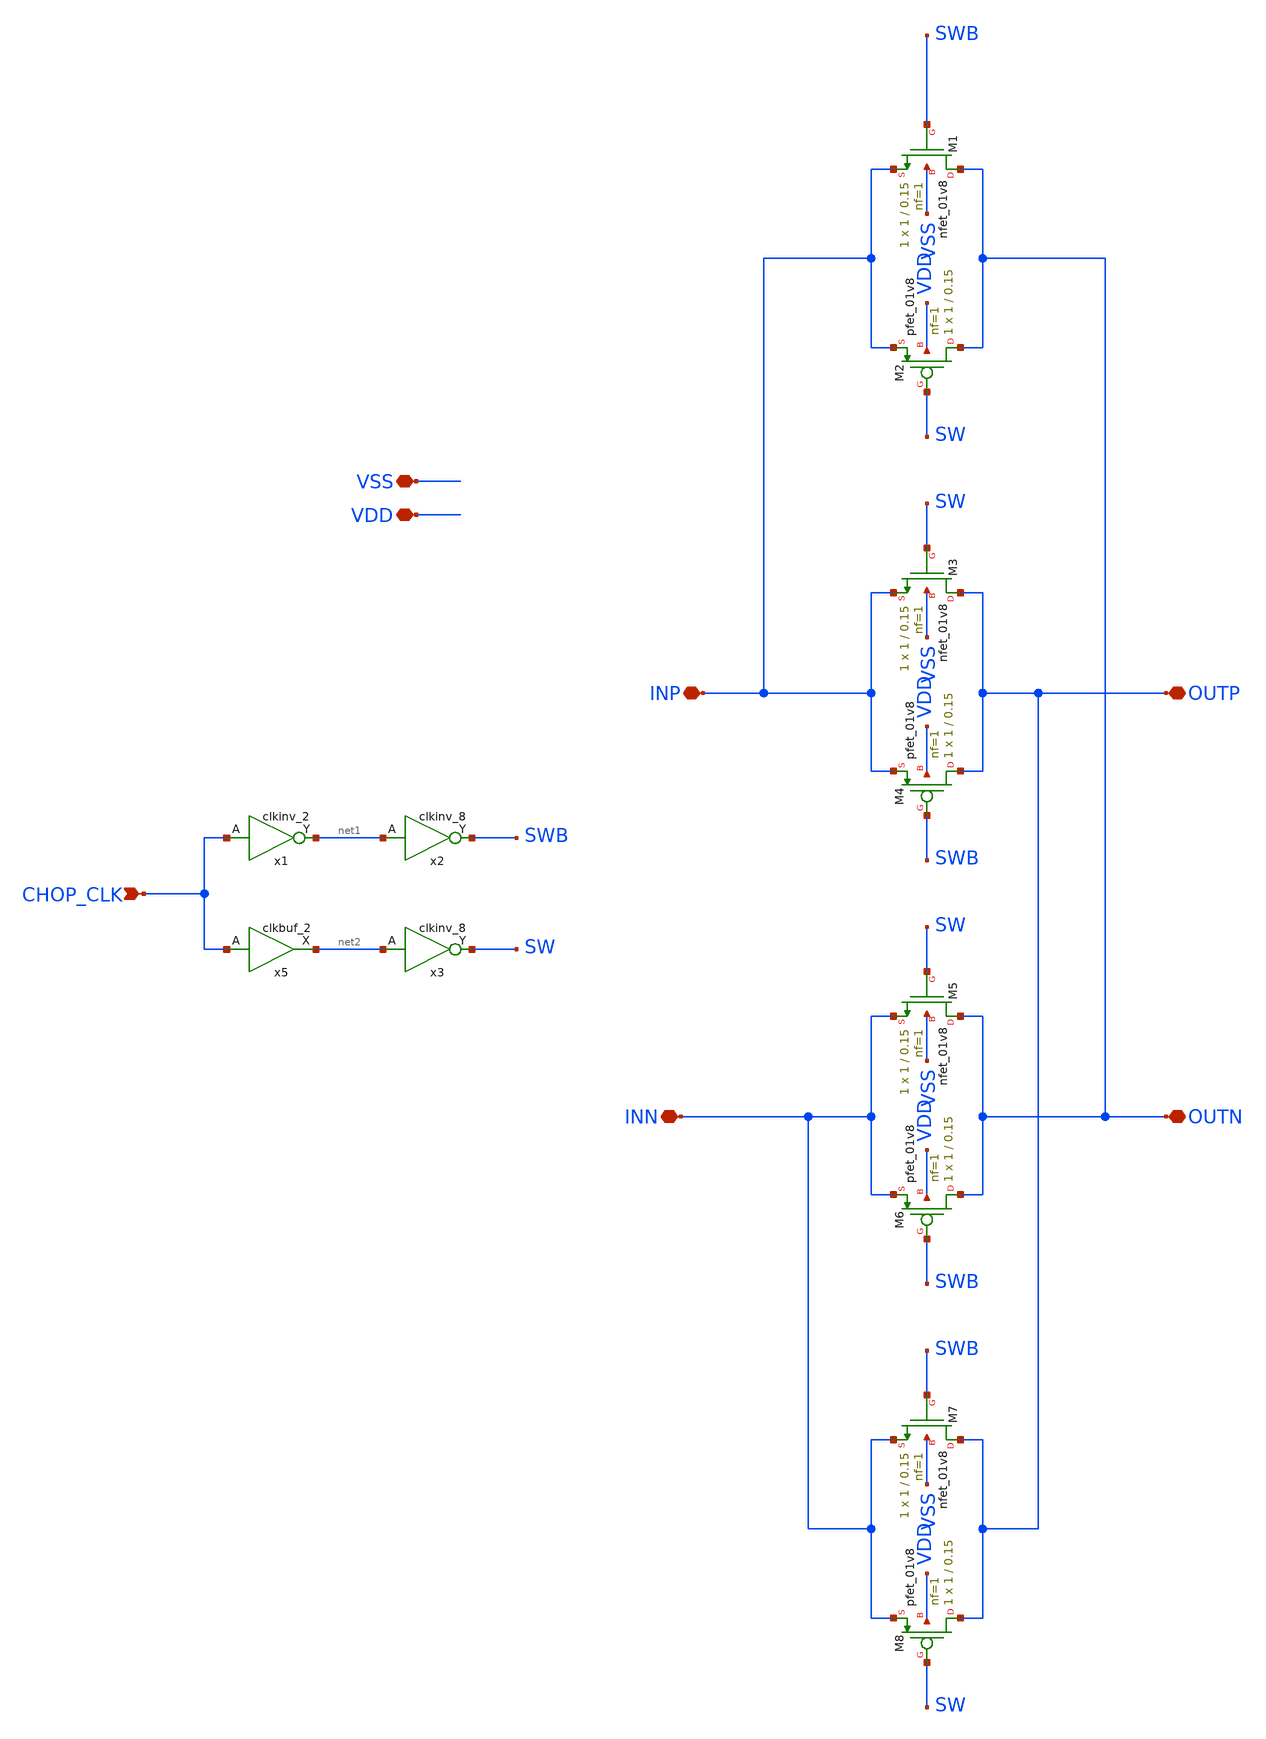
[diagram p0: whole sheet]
** sch_path: opamp_lna/chopper.sch
**.subckt chopper CHOP_CLK INP INN OUTP OUTN VSS VDD
*.ipin CHOP_CLK
*.iopin INP
*.iopin INN
*.iopin OUTP
*.iopin OUTN
*.iopin VSS
*.iopin VDD
XM1 OUTN SWB INP VSS sky130_fd_pr__nfet_01v8 L=0.15 W=1 nf=1 ad='int((nf+1)/2) * W/nf * 0.29' as='int((nf+2)/2) * W/nf * 0.29'
+ pd='2*int((nf+1)/2) * (W/nf + 0.29)' ps='2*int((nf+2)/2) * (W/nf + 0.29)' nrd='0.29 / W' nrs='0.29 / W'
+ sa=0 sb=0 sd=0 mult=1 m=1
XM2 OUTN SW INP VDD sky130_fd_pr__pfet_01v8 L=0.15 W=1 nf=1 ad='int((nf+1)/2) * W/nf * 0.29' as='int((nf+2)/2) * W/nf * 0.29'
+ pd='2*int((nf+1)/2) * (W/nf + 0.29)' ps='2*int((nf+2)/2) * (W/nf + 0.29)' nrd='0.29 / W' nrs='0.29 / W'
+ sa=0 sb=0 sd=0 mult=1 m=1
XM3 OUTP SW INP VSS sky130_fd_pr__nfet_01v8 L=0.15 W=1 nf=1 ad='int((nf+1)/2) * W/nf * 0.29' as='int((nf+2)/2) * W/nf * 0.29'
+ pd='2*int((nf+1)/2) * (W/nf + 0.29)' ps='2*int((nf+2)/2) * (W/nf + 0.29)' nrd='0.29 / W' nrs='0.29 / W'
+ sa=0 sb=0 sd=0 mult=1 m=1
XM4 OUTP SWB INP VDD sky130_fd_pr__pfet_01v8 L=0.15 W=1 nf=1 ad='int((nf+1)/2) * W/nf * 0.29' as='int((nf+2)/2) * W/nf * 0.29'
+ pd='2*int((nf+1)/2) * (W/nf + 0.29)' ps='2*int((nf+2)/2) * (W/nf + 0.29)' nrd='0.29 / W' nrs='0.29 / W'
+ sa=0 sb=0 sd=0 mult=1 m=1
XM5 OUTN SW INN VSS sky130_fd_pr__nfet_01v8 L=0.15 W=1 nf=1 ad='int((nf+1)/2) * W/nf * 0.29' as='int((nf+2)/2) * W/nf * 0.29'
+ pd='2*int((nf+1)/2) * (W/nf + 0.29)' ps='2*int((nf+2)/2) * (W/nf + 0.29)' nrd='0.29 / W' nrs='0.29 / W'
+ sa=0 sb=0 sd=0 mult=1 m=1
XM6 OUTN SWB INN VDD sky130_fd_pr__pfet_01v8 L=0.15 W=1 nf=1 ad='int((nf+1)/2) * W/nf * 0.29' as='int((nf+2)/2) * W/nf * 0.29'
+ pd='2*int((nf+1)/2) * (W/nf + 0.29)' ps='2*int((nf+2)/2) * (W/nf + 0.29)' nrd='0.29 / W' nrs='0.29 / W'
+ sa=0 sb=0 sd=0 mult=1 m=1
XM7 OUTP SWB INN VSS sky130_fd_pr__nfet_01v8 L=0.15 W=1 nf=1 ad='int((nf+1)/2) * W/nf * 0.29' as='int((nf+2)/2) * W/nf * 0.29'
+ pd='2*int((nf+1)/2) * (W/nf + 0.29)' ps='2*int((nf+2)/2) * (W/nf + 0.29)' nrd='0.29 / W' nrs='0.29 / W'
+ sa=0 sb=0 sd=0 mult=1 m=1
XM8 OUTP SW INN VDD sky130_fd_pr__pfet_01v8 L=0.15 W=1 nf=1 ad='int((nf+1)/2) * W/nf * 0.29' as='int((nf+2)/2) * W/nf * 0.29'
+ pd='2*int((nf+1)/2) * (W/nf + 0.29)' ps='2*int((nf+2)/2) * (W/nf + 0.29)' nrd='0.29 / W' nrs='0.29 / W'
+ sa=0 sb=0 sd=0 mult=1 m=1
x5 CHOP_CLK VSS VNB VPB VDD net2 sky130_fd_sc_hd__clkbuf_2
x1 CHOP_CLK VGND VNB VPB VPWR net1 sky130_fd_sc_hd__clkinv_2
x2 net1 VSS VNB VPB VDD SWB sky130_fd_sc_hd__clkinv_8
x3 net2 VSS VNB VPB VDD SW sky130_fd_sc_hd__clkinv_8
**** begin user architecture code

** opencircuitdesign pdks install
.lib $::SKYWATER_MODELS/sky130.lib.spice tt
.include $::SKYWATER_STDCELLS/sky130_fd_sc_hd.spice

**** end user architecture code
**.ends
.end
